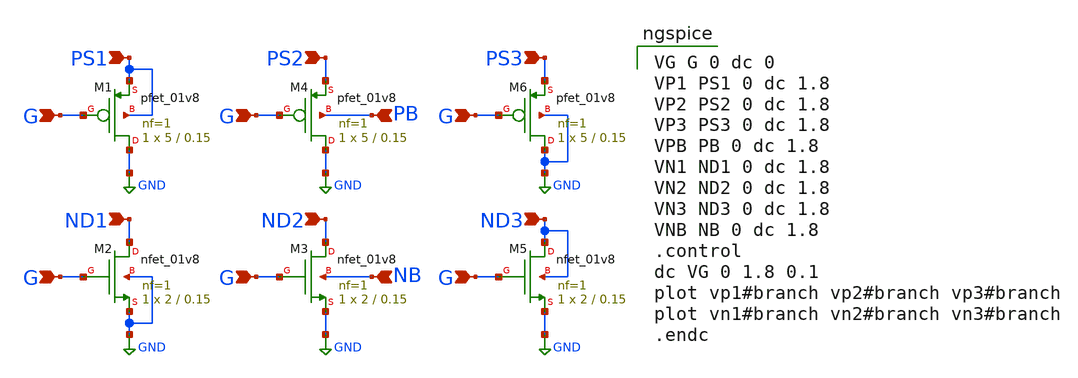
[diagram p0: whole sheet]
** sch_path: trbench2.sch
**.subckt trbench2 ND1 PS1 G G ND2 G NB PS2 G PB ND3 G PS3 G
*.ipin ND1
*.ipin PS1
*.ipin G
*.ipin G
*.ipin ND2
*.ipin G
*.ipin NB
*.ipin PS2
*.ipin G
*.ipin PB
*.ipin ND3
*.ipin G
*.ipin PS3
*.ipin G
XM1 GND G PS1 PS1 sky130_fd_pr__pfet_01v8 L=0.15 W=5 nf=1 ad='int((nf+1)/2) * W/nf * 0.29' as='int((nf+2)/2) * W/nf * 0.29'
+ pd='2*int((nf+1)/2) * (W/nf + 0.29)' ps='2*int((nf+2)/2) * (W/nf + 0.29)' nrd='0.29 / W' nrs='0.29 / W'
+ sa=0 sb=0 sd=0 mult=1 m=1
XM2 ND1 G GND GND sky130_fd_pr__nfet_01v8 L=0.15 W=2 nf=1 ad='int((nf+1)/2) * W/nf * 0.29' as='int((nf+2)/2) * W/nf * 0.29'
+ pd='2*int((nf+1)/2) * (W/nf + 0.29)' ps='2*int((nf+2)/2) * (W/nf + 0.29)' nrd='0.29 / W' nrs='0.29 / W'
+ sa=0 sb=0 sd=0 mult=1 m=1
XM3 ND2 G GND NB sky130_fd_pr__nfet_01v8 L=0.15 W=2 nf=1 ad='int((nf+1)/2) * W/nf * 0.29' as='int((nf+2)/2) * W/nf * 0.29'
+ pd='2*int((nf+1)/2) * (W/nf + 0.29)' ps='2*int((nf+2)/2) * (W/nf + 0.29)' nrd='0.29 / W' nrs='0.29 / W'
+ sa=0 sb=0 sd=0 mult=1 m=1
XM4 GND G PS2 PB sky130_fd_pr__pfet_01v8 L=0.15 W=5 nf=1 ad='int((nf+1)/2) * W/nf * 0.29' as='int((nf+2)/2) * W/nf * 0.29'
+ pd='2*int((nf+1)/2) * (W/nf + 0.29)' ps='2*int((nf+2)/2) * (W/nf + 0.29)' nrd='0.29 / W' nrs='0.29 / W'
+ sa=0 sb=0 sd=0 mult=1 m=1
XM5 ND3 G GND ND3 sky130_fd_pr__nfet_01v8 L=0.15 W=2 nf=1 ad='int((nf+1)/2) * W/nf * 0.29' as='int((nf+2)/2) * W/nf * 0.29'
+ pd='2*int((nf+1)/2) * (W/nf + 0.29)' ps='2*int((nf+2)/2) * (W/nf + 0.29)' nrd='0.29 / W' nrs='0.29 / W'
+ sa=0 sb=0 sd=0 mult=1 m=1
XM6 GND G PS3 GND sky130_fd_pr__pfet_01v8 L=0.15 W=5 nf=1 ad='int((nf+1)/2) * W/nf * 0.29' as='int((nf+2)/2) * W/nf * 0.29'
+ pd='2*int((nf+1)/2) * (W/nf + 0.29)' ps='2*int((nf+2)/2) * (W/nf + 0.29)' nrd='0.29 / W' nrs='0.29 / W'
+ sa=0 sb=0 sd=0 mult=1 m=1
**** begin user architecture code

VG G 0 dc 0
VP1 PS1 0 dc 1.8
VP2 PS2 0 dc 1.8
VP3 PS3 0 dc 1.8
VPB PB 0 dc 1.8
VN1 ND1 0 dc 1.8
VN2 ND2 0 dc 1.8
VN3 ND3 0 dc 1.8
VNB NB 0 dc 1.8
.control
dc VG 0 1.8 0.1
plot vp1#branch vp2#branch vp3#branch
plot vn1#branch vn2#branch vn3#branch
.endc


** opencircuitdesign pdks install
.lib $::SKYWATER_MODELS/sky130.lib.spice tt


**** end user architecture code
**.ends
.GLOBAL GND
.end
